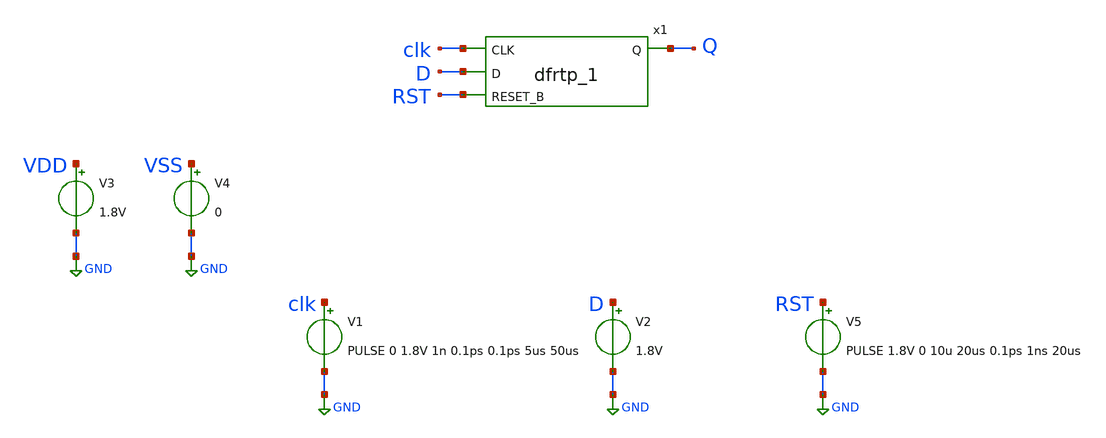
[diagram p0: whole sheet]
** sch_path: xschem/tests/dummy_tests/dummy_reset_threshold.sch
**.subckt dummy_reset_threshold
V3 VDD GND 1.8V
V4 VSS GND 0
V1 clk GND PULSE 0 1.8V 1n 0.1ps 0.1ps 5us 50us
V2 D GND 1.8V
x1 clk D RST VSS VSS VDD VDD Q sky130_fd_sc_hd__dfrtp_1
V5 RST GND PULSE 1.8V 0 10u 20us 0.1ps 1ns 20us
**** begin user architecture code
 .lib $::SKYWATER_MODELS/sky130.lib.spice tt
.include $::SKYWATER_STDCELLS/sky130_fd_sc_hd.spice


.options acct list
.temp 25
*vvcc VDD 0 dc 1.8
*vvss VSS 0 0
.control
tran 0.1u 40us
*plot RST_PLS clk+2 Pulse+4
plot clk D+2 Q+4 RST+4
write dummy.raw
.endc


**** end user architecture code
**.ends
.GLOBAL GND
.end
